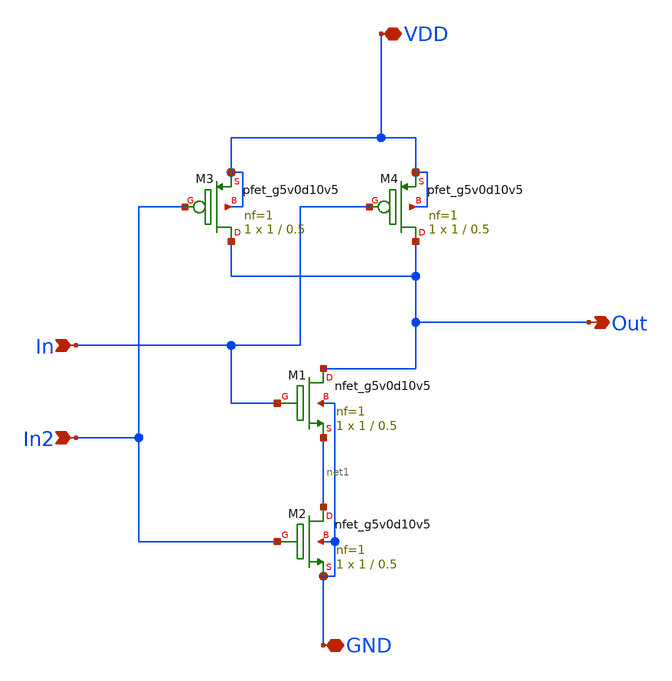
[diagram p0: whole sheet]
** sch_path: Analog Design Alan Rivera/Xschem/Sch/nand.sch
**.subckt nand In VDD Out In2 GND
*.ipin In
*.iopin VDD
*.opin Out
*.ipin In2
*.iopin GND
XM2 net1 In2 GND GND sky130_fd_pr__nfet_g5v0d10v5 L=0.5 W=1 nf=1 ad='int((nf+1)/2) * W/nf * 0.29' as='int((nf+2)/2) * W/nf * 0.29'
+ pd='2*int((nf+1)/2) * (W/nf + 0.29)' ps='2*int((nf+2)/2) * (W/nf + 0.29)' nrd='0.29 / W' nrs='0.29 / W'
+ sa=0 sb=0 sd=0 mult=1 m=1
XM1 Out In net1 GND sky130_fd_pr__nfet_g5v0d10v5 L=0.5 W=1 nf=1 ad='int((nf+1)/2) * W/nf * 0.29' as='int((nf+2)/2) * W/nf * 0.29'
+ pd='2*int((nf+1)/2) * (W/nf + 0.29)' ps='2*int((nf+2)/2) * (W/nf + 0.29)' nrd='0.29 / W' nrs='0.29 / W'
+ sa=0 sb=0 sd=0 mult=1 m=1
XM3 Out In2 VDD VDD sky130_fd_pr__pfet_g5v0d10v5 L=0.5 W=1 nf=1 ad='int((nf+1)/2) * W/nf * 0.29' as='int((nf+2)/2) * W/nf * 0.29'
+ pd='2*int((nf+1)/2) * (W/nf + 0.29)' ps='2*int((nf+2)/2) * (W/nf + 0.29)' nrd='0.29 / W' nrs='0.29 / W'
+ sa=0 sb=0 sd=0 mult=1 m=1
XM4 Out In VDD VDD sky130_fd_pr__pfet_g5v0d10v5 L=0.5 W=1 nf=1 ad='int((nf+1)/2) * W/nf * 0.29' as='int((nf+2)/2) * W/nf * 0.29'
+ pd='2*int((nf+1)/2) * (W/nf + 0.29)' ps='2*int((nf+2)/2) * (W/nf + 0.29)' nrd='0.29 / W' nrs='0.29 / W'
+ sa=0 sb=0 sd=0 mult=1 m=1
**.ends
.end
